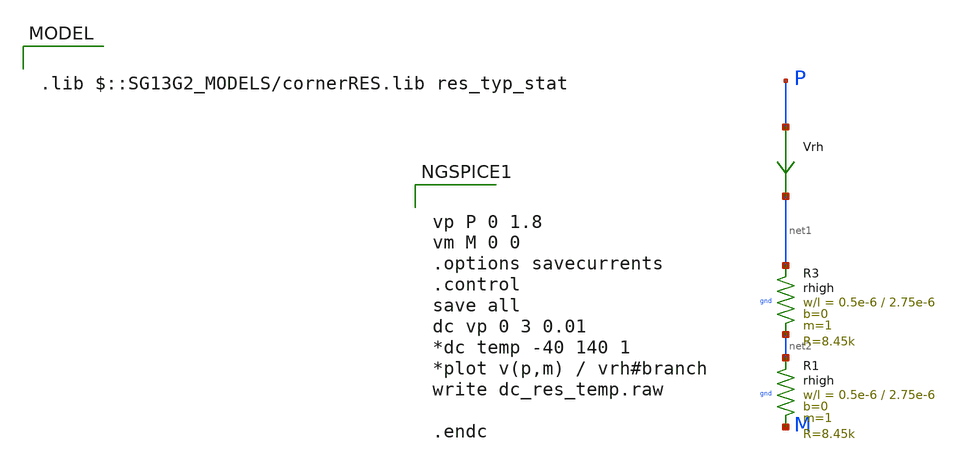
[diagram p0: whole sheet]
** sch_path: schematic/test5.sch
**.subckt test5
Vrh P net1 0
.save i(vrh)
XR3 net1 net2 gnd rhigh w=0.5e-6 l=2.75e-6 m=1 b=0 mm_ok=1
XR1 net2 M gnd rhigh w=0.5e-6 l=2.75e-6 m=1 b=0 mm_ok=1
**** begin user architecture code

.lib $::SG13G2_MODELS/cornerRES.lib res_typ_stat



vp P 0 1.8
vm M 0 0
.options savecurrents
.control
save all
dc vp 0 3 0.01
*dc temp -40 140 1
*plot v(p,m) / vrh#branch
write dc_res_temp.raw

.endc


**** end user architecture code
**.ends
.end
